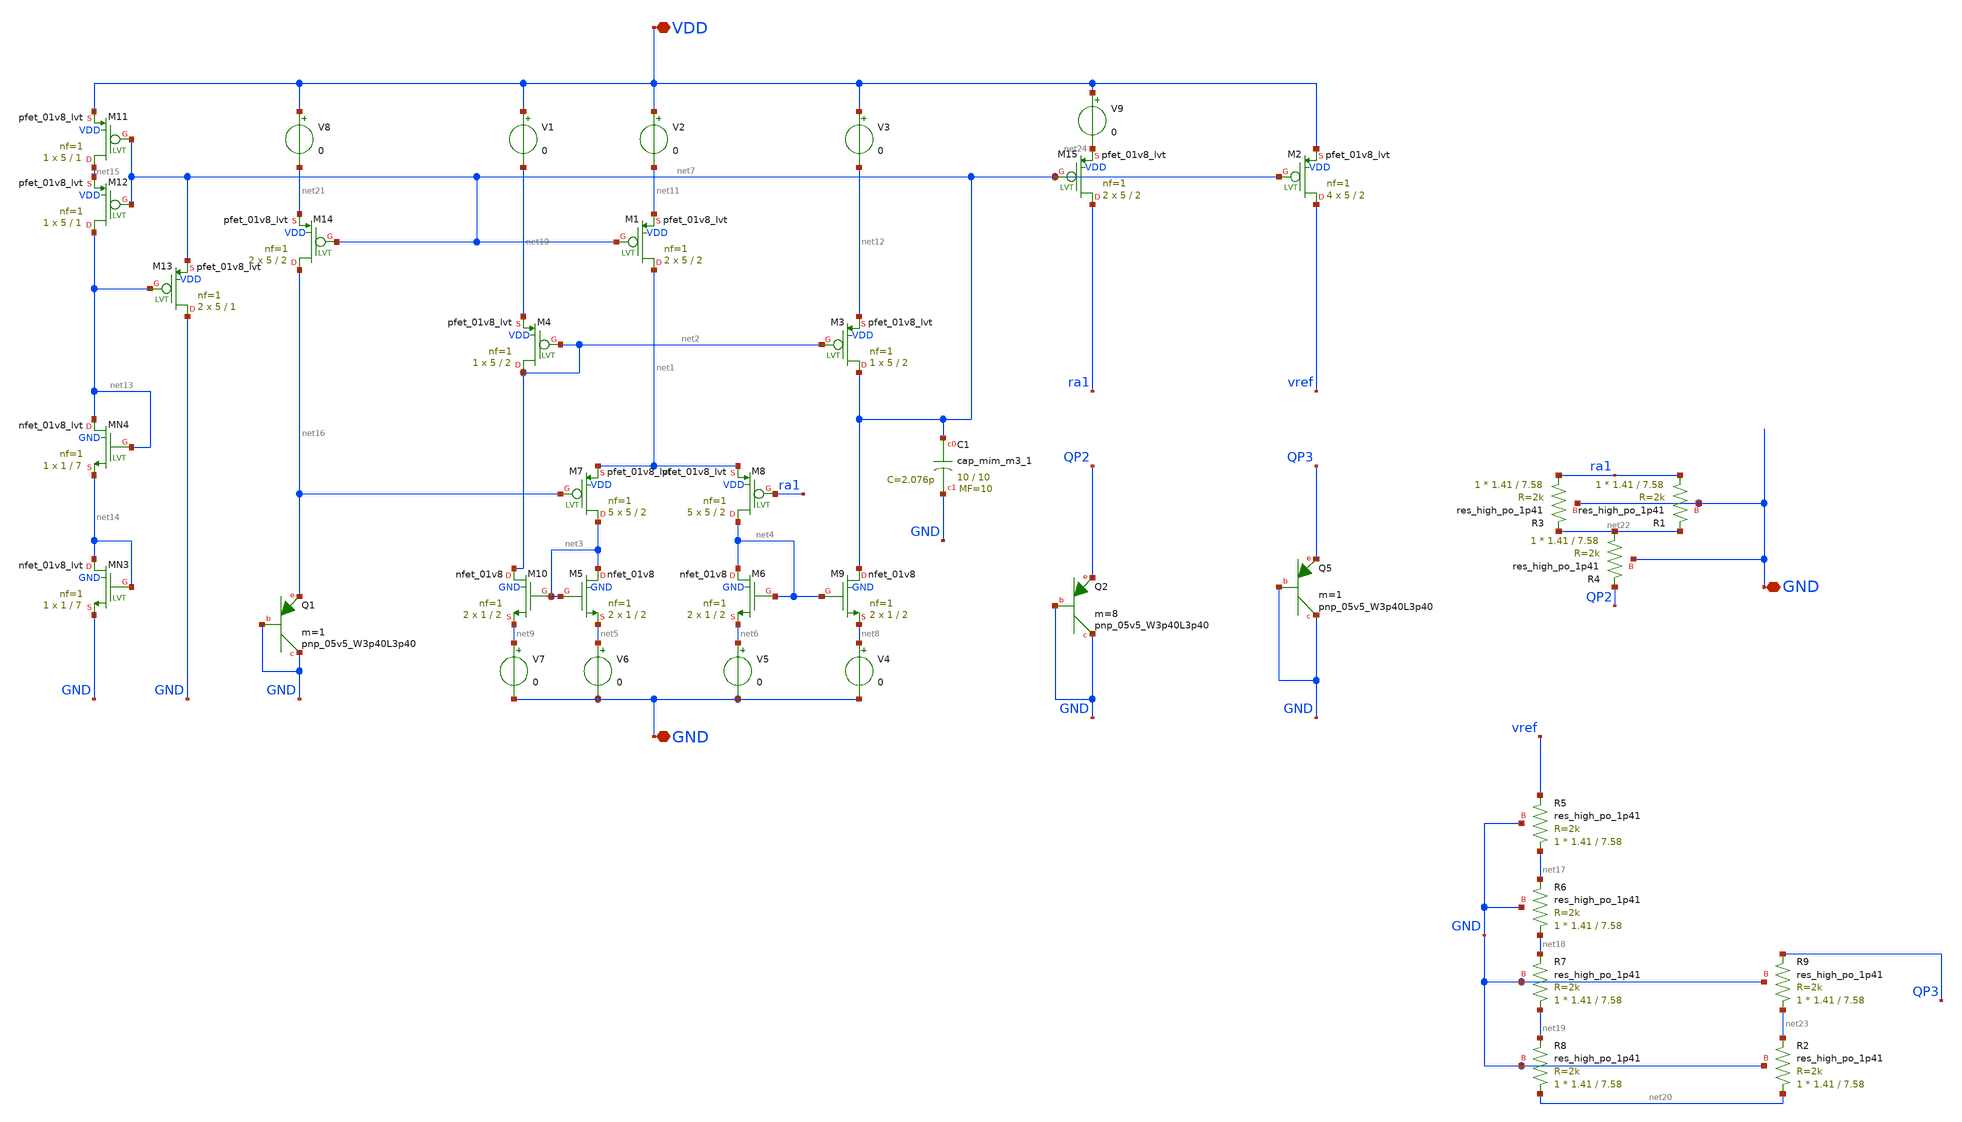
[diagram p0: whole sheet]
** sch_path: NES-2026/STDCELLS/xschem/BGR_opamp.sch
**.subckt BGR_opamp VDD GND GND
*.iopin VDD
*.iopin GND
*.iopin GND
XM1 net1 net7 net11 VDD sky130_fd_pr__pfet_01v8_lvt L=2 W=5 nf=1 ad='int((1 + 1)/2) * 5 / 1 * 0.29' as='int((1 + 2)/2) * 5 / 1 * 0.29'
+ pd='2*int((1 + 1)/2) * (5 / 1 + 0.29)' ps='2*int((1 + 2)/2) * (5 / 1 + 0.29)' nrd='0.29 / 5 ' nrs='0.29 / 5 '
+ sa=0 sb=0 sd=0 mult=2 m=2
XM3 net7 net2 net12 VDD sky130_fd_pr__pfet_01v8_lvt L=2 W=5 nf=1 ad='int((1 + 1)/2) * 5 / 1 * 0.29' as='int((1 + 2)/2) * 5 / 1 * 0.29'
+ pd='2*int((1 + 1)/2) * (5 / 1 + 0.29)' ps='2*int((1 + 2)/2) * (5 / 1 + 0.29)' nrd='0.29 / 5 ' nrs='0.29 / 5 '
+ sa=0 sb=0 sd=0 mult=1 m=1
XM4 net2 net2 net10 VDD sky130_fd_pr__pfet_01v8_lvt L=2 W=5 nf=1 ad='int((1 + 1)/2) * 5 / 1 * 0.29' as='int((1 + 2)/2) * 5 / 1 * 0.29'
+ pd='2*int((1 + 1)/2) * (5 / 1 + 0.29)' ps='2*int((1 + 2)/2) * (5 / 1 + 0.29)' nrd='0.29 / 5 ' nrs='0.29 / 5 '
+ sa=0 sb=0 sd=0 mult=1 m=1
XM5 net3 net3 net5 GND sky130_fd_pr__nfet_01v8 L=2 W=1 nf=1 ad='int((1 + 1)/2) * 1 / 1 * 0.29' as='int((1 + 2)/2) * 1 / 1 * 0.29'
+ pd='2*int((1 + 1)/2) * (1 / 1 + 0.29)' ps='2*int((1 + 2)/2) * (1 / 1 + 0.29)' nrd='0.29 / 1 ' nrs='0.29 / 1 '
+ sa=0 sb=0 sd=0 mult=2 m=2
XM6 net4 net4 net6 GND sky130_fd_pr__nfet_01v8 L=2 W=1 nf=1 ad='int((1 + 1)/2) * 1 / 1 * 0.29' as='int((1 + 2)/2) * 1 / 1 * 0.29'
+ pd='2*int((1 + 1)/2) * (1 / 1 + 0.29)' ps='2*int((1 + 2)/2) * (1 / 1 + 0.29)' nrd='0.29 / 1 ' nrs='0.29 / 1 '
+ sa=0 sb=0 sd=0 mult=2 m=2
XM7 net3 net16 net1 VDD sky130_fd_pr__pfet_01v8_lvt L=2 W=5 nf=1 ad='int((1 + 1)/2) * 5 / 1 * 0.29' as='int((1 + 2)/2) * 5 / 1 * 0.29'
+ pd='2*int((1 + 1)/2) * (5 / 1 + 0.29)' ps='2*int((1 + 2)/2) * (5 / 1 + 0.29)' nrd='0.29 / 5 ' nrs='0.29 / 5 '
+ sa=0 sb=0 sd=0 mult=5 m=5
XM8 net4 ra1 net1 VDD sky130_fd_pr__pfet_01v8_lvt L=2 W=5 nf=1 ad='int((1 + 1)/2) * 5 / 1 * 0.29' as='int((1 + 2)/2) * 5 / 1 * 0.29'
+ pd='2*int((1 + 1)/2) * (5 / 1 + 0.29)' ps='2*int((1 + 2)/2) * (5 / 1 + 0.29)' nrd='0.29 / 5 ' nrs='0.29 / 5 '
+ sa=0 sb=0 sd=0 mult=5 m=5
XM9 net7 net4 net8 GND sky130_fd_pr__nfet_01v8 L=2 W=1 nf=1 ad='int((1 + 1)/2) * 1 / 1 * 0.29' as='int((1 + 2)/2) * 1 / 1 * 0.29'
+ pd='2*int((1 + 1)/2) * (1 / 1 + 0.29)' ps='2*int((1 + 2)/2) * (1 / 1 + 0.29)' nrd='0.29 / 1 ' nrs='0.29 / 1 '
+ sa=0 sb=0 sd=0 mult=2 m=2
XM10 net2 net3 net9 GND sky130_fd_pr__nfet_01v8 L=2 W=1 nf=1 ad='int((1 + 1)/2) * 1 / 1 * 0.29' as='int((1 + 2)/2) * 1 / 1 * 0.29'
+ pd='2*int((1 + 1)/2) * (1 / 1 + 0.29)' ps='2*int((1 + 2)/2) * (1 / 1 + 0.29)' nrd='0.29 / 1 ' nrs='0.29 / 1 '
+ sa=0 sb=0 sd=0 mult=2 m=2
XC1 net7 GND sky130_fd_pr__cap_mim_m3_1 W=10 L=10 MF=10 m=10
V1 VDD net10 0
V2 VDD net11 0
V3 VDD net12 0
V4 net8 GND 0
V5 net6 GND 0
V6 net5 GND 0
V7 net9 GND 0
XM11 net15 net7 VDD VDD sky130_fd_pr__pfet_01v8_lvt L=1 W=5 nf=1 ad='int((1 + 1)/2) * 5 / 1 * 0.29' as='int((1 + 2)/2) * 5 / 1 * 0.29'
+ pd='2*int((1 + 1)/2) * (5 / 1 + 0.29)' ps='2*int((1 + 2)/2) * (5 / 1 + 0.29)' nrd='0.29 / 5 ' nrs='0.29 / 5 '
+ sa=0 sb=0 sd=0 mult=1 m=1
XM12 net13 net7 net15 VDD sky130_fd_pr__pfet_01v8_lvt L=1 W=5 nf=1 ad='int((1 + 1)/2) * 5 / 1 * 0.29'
+ as='int((1 + 2)/2) * 5 / 1 * 0.29' pd='2*int((1 + 1)/2) * (5 / 1 + 0.29)' ps='2*int((1 + 2)/2) * (5 / 1 + 0.29)'
+ nrd='0.29 / 5 ' nrs='0.29 / 5 ' sa=0 sb=0 sd=0 mult=1 m=1
XM13 GND net13 net7 VDD sky130_fd_pr__pfet_01v8_lvt L=1 W=5 nf=1 ad='int((1 + 1)/2) * 5 / 1 * 0.29' as='int((1 + 2)/2) * 5 / 1 * 0.29'
+ pd='2*int((1 + 1)/2) * (5 / 1 + 0.29)' ps='2*int((1 + 2)/2) * (5 / 1 + 0.29)' nrd='0.29 / 5 ' nrs='0.29 / 5 '
+ sa=0 sb=0 sd=0 mult=2 m=2
XMN3 net14 net14 GND GND sky130_fd_pr__nfet_01v8_lvt L=7 W=1 nf=1 ad='int((1 + 1)/2) * 1 / 1 * 0.29'
+ as='int((1 + 2)/2) * 1 / 1 * 0.29' pd='2*int((1 + 1)/2) * (1 / 1 + 0.29)' ps='2*int((1 + 2)/2) * (1 / 1 + 0.29)'
+ nrd='0.29 / 1 ' nrs='0.29 / 1 ' sa=0 sb=0 sd=0 mult=1 m=1
XMN4 net13 net13 net14 GND sky130_fd_pr__nfet_01v8_lvt L=7 W=1 nf=1 ad='int((1 + 1)/2) * 1 / 1 * 0.29'
+ as='int((1 + 2)/2) * 1 / 1 * 0.29' pd='2*int((1 + 1)/2) * (1 / 1 + 0.29)' ps='2*int((1 + 2)/2) * (1 / 1 + 0.29)'
+ nrd='0.29 / 1 ' nrs='0.29 / 1 ' sa=0 sb=0 sd=0 mult=1 m=1
XQ1 GND GND net16 sky130_fd_pr__pnp_05v5_W3p40L3p40 m=1
XM14 net16 net7 net21 VDD sky130_fd_pr__pfet_01v8_lvt L=2 W=5 nf=1 ad='int((1 + 1)/2) * 5 / 1 * 0.29'
+ as='int((1 + 2)/2) * 5 / 1 * 0.29' pd='2*int((1 + 1)/2) * (5 / 1 + 0.29)' ps='2*int((1 + 2)/2) * (5 / 1 + 0.29)'
+ nrd='0.29 / 5 ' nrs='0.29 / 5 ' sa=0 sb=0 sd=0 mult=2 m=2
XM15 ra1 net7 net24 VDD sky130_fd_pr__pfet_01v8_lvt L=2 W=5 nf=1 ad='int((1 + 1)/2) * 5 / 1 * 0.29' as='int((1 + 2)/2) * 5 / 1 * 0.29'
+ pd='2*int((1 + 1)/2) * (5 / 1 + 0.29)' ps='2*int((1 + 2)/2) * (5 / 1 + 0.29)' nrd='0.29 / 5 ' nrs='0.29 / 5 '
+ sa=0 sb=0 sd=0 mult=2 m=2
XR3 ra1 net22 GND sky130_fd_pr__res_high_po_1p41 L=7.58 mult=1 m=1
XQ2 GND GND QP2 sky130_fd_pr__pnp_05v5_W3p40L3p40 m=8
XR5 net17 vref GND sky130_fd_pr__res_high_po_1p41 L=7.58 mult=1 m=1
XR6 net18 net17 GND sky130_fd_pr__res_high_po_1p41 L=7.58 mult=1 m=1
XR7 net19 net18 GND sky130_fd_pr__res_high_po_1p41 L=7.58 mult=1 m=1
XR8 net20 net19 GND sky130_fd_pr__res_high_po_1p41 L=7.58 mult=1 m=1
XM2 vref net7 VDD VDD sky130_fd_pr__pfet_01v8_lvt L=2 W=5 nf=1 ad='int((1 + 1)/2) * 5 / 1 * 0.29' as='int((1 + 2)/2) * 5 / 1 * 0.29'
+ pd='2*int((1 + 1)/2) * (5 / 1 + 0.29)' ps='2*int((1 + 2)/2) * (5 / 1 + 0.29)' nrd='0.29 / 5 ' nrs='0.29 / 5 '
+ sa=0 sb=0 sd=0 mult=4 m=4
XQ5 GND GND QP3 sky130_fd_pr__pnp_05v5_W3p40L3p40 m=1
V8 VDD net21 0
V9 VDD net24 0
XR1 ra1 net22 GND sky130_fd_pr__res_high_po_1p41 L=7.58 mult=1 m=1
XR2 net20 net23 GND sky130_fd_pr__res_high_po_1p41 L=7.58 mult=1 m=1
XR4 net22 QP2 GND sky130_fd_pr__res_high_po_1p41 L=7.58 mult=1 m=1
XR9 net23 QP3 GND sky130_fd_pr__res_high_po_1p41 L=7.58 mult=1 m=1
**** begin user architecture code

.title BGR_opamp
.lib /home/somya/share/pdk/sky130A/libs.tech/ngspice/sky130.lib.spice tt
.temp 27
.global VDD GND
.dc vin 0 1.8 0.01
.save all

vsup    VDD     GND     dc      2
.dc temp -40 125 5

*vsup   vdd     gnd     pulse   0       2       10n     1u      1u      1m      100u
*.tran  5n      10u

.control
run
plot v(vref)
*PLOT v(M7gate) v(ra1) v(QP2)
*plot vid1#branch vid2#branch vid3#branch vid4#branch vid5#branch
*plot i(V1) i(V2) i(V3) i(V8) i(V9)
.endc
.end


**** end user architecture code
**.ends
.end
